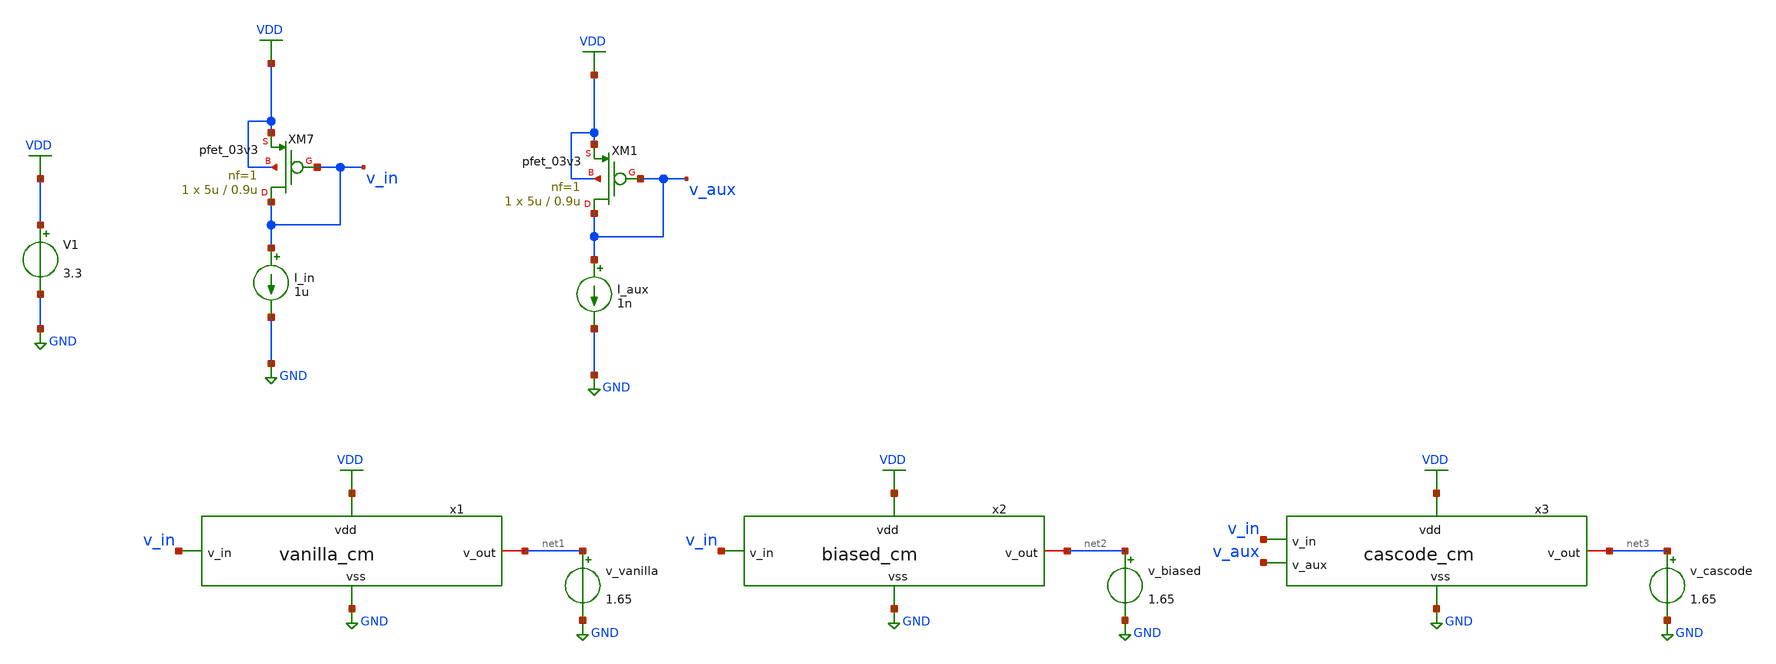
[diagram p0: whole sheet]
** sch_path: blocks/composite/regulated_cascoded_cmirror/xschem/testbench.sch
**.subckt testbench
V1 VDD GND 3.3
XM7 v_in v_in VDD VDD pfet_03v3 L=0.9u W=5u nf=1 ad='int((nf+1)/2) * W/nf * 0.18u' as='int((nf+2)/2) * W/nf * 0.18u'
+ pd='2*int((nf+1)/2) * (W/nf + 0.18u)' ps='2*int((nf+2)/2) * (W/nf + 0.18u)' nrd='0.18u / W' nrs='0.18u / W'
+ sa=0 sb=0 sd=0 m=1
I_in v_in GND 1u
x1 VDD v_in net1 GND vanilla_cm
v_vanilla net1 GND 1.65
.save i(v_vanilla)
x2 VDD v_in net2 GND biased_cm
v_biased net2 GND 1.65
.save i(v_biased)
x3 v_aux VDD v_in net3 GND cascode_cm
v_cascode net3 GND 1.65
.save i(v_cascode)
XM1 v_aux v_aux VDD VDD pfet_03v3 L=0.9u W=5u nf=1 ad='int((nf+1)/2) * W/nf * 0.18u' as='int((nf+2)/2) * W/nf * 0.18u'
+ pd='2*int((nf+1)/2) * (W/nf + 0.18u)' ps='2*int((nf+2)/2) * (W/nf + 0.18u)' nrd='0.18u / W' nrs='0.18u / W'
+ sa=0 sb=0 sd=0 m=1
I_aux v_aux GND 1n
**** begin user architecture code

.include /foss/pdks/gf180mcuD/libs.tech/ngspice/design.ngspice
.lib /foss/pdks/gf180mcuD/libs.tech/ngspice/sm141064.ngspice typical




.option savecurrent

.control

save all

* --- Run vanilla sweep ---
dc v_vanilla 0 3.3 0.01
let i_vanilla = -i(v_vanilla)
wrdata vanilla.txt i_vanilla

* --- Run biased sweep ---
reset
dc v_biased 0 3.3 0.01
let i_biased = -i(v_biased)
wrdata biased.txt i_biased

* --- Run cascode sweep ---
reset
dc v_cascode 0 3.3 0.01
let i_cascode = -i(v_cascode)
wrdata cascode.txt i_cascode

.endc


**** end user architecture code
**.ends

* expanding   symbol:  vanilla_cm.sym # of pins=4
** sym_path: blocks/composite/regulated_cascoded_cmirror/xschem/vanilla_cm.sym
** sch_path: blocks/composite/regulated_cascoded_cmirror/xschem/vanilla_cm.sch
.subckt vanilla_cm vdd v_in v_out vss
*.ipin v_in
*.ipin vdd
*.ipin vss
*.iopin v_out
XM1 v_out net1 vss vss nfet_03v3 L=0.9u W=5u nf=1 ad='int((nf+1)/2) * W/nf * 0.18u' as='int((nf+2)/2) * W/nf * 0.18u'
+ pd='2*int((nf+1)/2) * (W/nf + 0.18u)' ps='2*int((nf+2)/2) * (W/nf + 0.18u)' nrd='0.18u / W' nrs='0.18u / W'
+ sa=0 sb=0 sd=0 m=1
XM2 net1 net1 vss vss nfet_03v3 L=0.9u W=5u nf=1 ad='int((nf+1)/2) * W/nf * 0.18u' as='int((nf+2)/2) * W/nf * 0.18u'
+ pd='2*int((nf+1)/2) * (W/nf + 0.18u)' ps='2*int((nf+2)/2) * (W/nf + 0.18u)' nrd='0.18u / W' nrs='0.18u / W'
+ sa=0 sb=0 sd=0 m=1
XM9 net1 v_in vdd vdd pfet_03v3 L=0.9u W=5u nf=1 ad='int((nf+1)/2) * W/nf * 0.18u' as='int((nf+2)/2) * W/nf * 0.18u'
+ pd='2*int((nf+1)/2) * (W/nf + 0.18u)' ps='2*int((nf+2)/2) * (W/nf + 0.18u)' nrd='0.18u / W' nrs='0.18u / W'
+ sa=0 sb=0 sd=0 m=1
.ends


* expanding   symbol:  biased_cm.sym # of pins=4
** sym_path: blocks/composite/regulated_cascoded_cmirror/xschem/biased_cm.sym
** sch_path: blocks/composite/regulated_cascoded_cmirror/xschem/biased_cm.sch
.subckt biased_cm vdd v_in v_out vss
*.ipin v_in
*.ipin vdd
*.ipin vss
*.iopin v_out
XM3 net2 net1 vss vss nfet_03v3 L=0.9u W=5u nf=1 ad='int((nf+1)/2) * W/nf * 0.18u' as='int((nf+2)/2) * W/nf * 0.18u'
+ pd='2*int((nf+1)/2) * (W/nf + 0.18u)' ps='2*int((nf+2)/2) * (W/nf + 0.18u)' nrd='0.18u / W' nrs='0.18u / W'
+ sa=0 sb=0 sd=0 m=1
XM4 net1 net1 vss vss nfet_03v3 L=0.9u W=5u nf=1 ad='int((nf+1)/2) * W/nf * 0.18u' as='int((nf+2)/2) * W/nf * 0.18u'
+ pd='2*int((nf+1)/2) * (W/nf + 0.18u)' ps='2*int((nf+2)/2) * (W/nf + 0.18u)' nrd='0.18u / W' nrs='0.18u / W'
+ sa=0 sb=0 sd=0 m=1
XM5 v_out net3 net2 net2 nfet_03v3 L=0.9u W=5u nf=1 ad='int((nf+1)/2) * W/nf * 0.18u' as='int((nf+2)/2) * W/nf * 0.18u'
+ pd='2*int((nf+1)/2) * (W/nf + 0.18u)' ps='2*int((nf+2)/2) * (W/nf + 0.18u)' nrd='0.18u / W' nrs='0.18u / W'
+ sa=0 sb=0 sd=0 m=1
XM6 net3 net3 net1 net1 nfet_03v3 L=0.9u W=5u nf=1 ad='int((nf+1)/2) * W/nf * 0.18u' as='int((nf+2)/2) * W/nf * 0.18u'
+ pd='2*int((nf+1)/2) * (W/nf + 0.18u)' ps='2*int((nf+2)/2) * (W/nf + 0.18u)' nrd='0.18u / W' nrs='0.18u / W'
+ sa=0 sb=0 sd=0 m=1
XM15 net3 v_in vdd vdd pfet_03v3 L=0.9u W=5u nf=1 ad='int((nf+1)/2) * W/nf * 0.18u' as='int((nf+2)/2) * W/nf * 0.18u'
+ pd='2*int((nf+1)/2) * (W/nf + 0.18u)' ps='2*int((nf+2)/2) * (W/nf + 0.18u)' nrd='0.18u / W' nrs='0.18u / W'
+ sa=0 sb=0 sd=0 m=1
.ends


* expanding   symbol:  cascode_cm.sym # of pins=5
** sym_path: blocks/composite/regulated_cascoded_cmirror/xschem/cascode_cm.sym
** sch_path: blocks/composite/regulated_cascoded_cmirror/xschem/cascode_cm.sch
.subckt cascode_cm v_aux vdd v_in v_out vss
*.ipin v_in
*.ipin vdd
*.ipin vss
*.ipin v_aux
*.iopin v_out
XM10 net2 net1 vss vss nfet_03v3 L=0.9u W=2u nf=1 ad='int((nf+1)/2) * W/nf * 0.18u' as='int((nf+2)/2) * W/nf * 0.18u'
+ pd='2*int((nf+1)/2) * (W/nf + 0.18u)' ps='2*int((nf+2)/2) * (W/nf + 0.18u)' nrd='0.18u / W' nrs='0.18u / W'
+ sa=0 sb=0 sd=0 m=1
XM8 net4 net2 net1 net1 nfet_03v3 L=0.9u W=2u nf=1 ad='int((nf+1)/2) * W/nf * 0.18u' as='int((nf+2)/2) * W/nf * 0.18u'
+ pd='2*int((nf+1)/2) * (W/nf + 0.18u)' ps='2*int((nf+2)/2) * (W/nf + 0.18u)' nrd='0.18u / W' nrs='0.18u / W'
+ sa=0 sb=0 sd=0 m=1
XM11 net1 net4 vss vss nfet_03v3 L=0.9u W=2u nf=1 ad='int((nf+1)/2) * W/nf * 0.18u' as='int((nf+2)/2) * W/nf * 0.18u'
+ pd='2*int((nf+1)/2) * (W/nf + 0.18u)' ps='2*int((nf+2)/2) * (W/nf + 0.18u)' nrd='0.18u / W' nrs='0.18u / W'
+ sa=0 sb=0 sd=0 m=1
XM12 net2 net3 vss vss nfet_03v3 L=0.9u W=2u nf=1 ad='int((nf+1)/2) * W/nf * 0.18u' as='int((nf+2)/2) * W/nf * 0.18u'
+ pd='2*int((nf+1)/2) * (W/nf + 0.18u)' ps='2*int((nf+2)/2) * (W/nf + 0.18u)' nrd='0.18u / W' nrs='0.18u / W'
+ sa=0 sb=0 sd=0 m=1
XM13 net3 net4 vss vss nfet_03v3 L=0.9u W=2u nf=1 ad='int((nf+1)/2) * W/nf * 0.18u' as='int((nf+2)/2) * W/nf * 0.18u'
+ pd='2*int((nf+1)/2) * (W/nf + 0.18u)' ps='2*int((nf+2)/2) * (W/nf + 0.18u)' nrd='0.18u / W' nrs='0.18u / W'
+ sa=0 sb=0 sd=0 m=1
XM14 v_out net2 net3 net3 nfet_03v3 L=0.9u W=2u nf=1 ad='int((nf+1)/2) * W/nf * 0.18u' as='int((nf+2)/2) * W/nf * 0.18u'
+ pd='2*int((nf+1)/2) * (W/nf + 0.18u)' ps='2*int((nf+2)/2) * (W/nf + 0.18u)' nrd='0.18u / W' nrs='0.18u / W'
+ sa=0 sb=0 sd=0 m=1
XM16 net4 v_in vdd vdd pfet_03v3 L=0.9u W=5u nf=1 ad='int((nf+1)/2) * W/nf * 0.18u' as='int((nf+2)/2) * W/nf * 0.18u'
+ pd='2*int((nf+1)/2) * (W/nf + 0.18u)' ps='2*int((nf+2)/2) * (W/nf + 0.18u)' nrd='0.18u / W' nrs='0.18u / W'
+ sa=0 sb=0 sd=0 m=1
XM18 net2 v_aux vdd vdd pfet_03v3 L=0.9u W=5u nf=1 ad='int((nf+1)/2) * W/nf * 0.18u' as='int((nf+2)/2) * W/nf * 0.18u'
+ pd='2*int((nf+1)/2) * (W/nf + 0.18u)' ps='2*int((nf+2)/2) * (W/nf + 0.18u)' nrd='0.18u / W' nrs='0.18u / W'
+ sa=0 sb=0 sd=0 m=1
.ends

.GLOBAL VDD
.GLOBAL GND
.end
